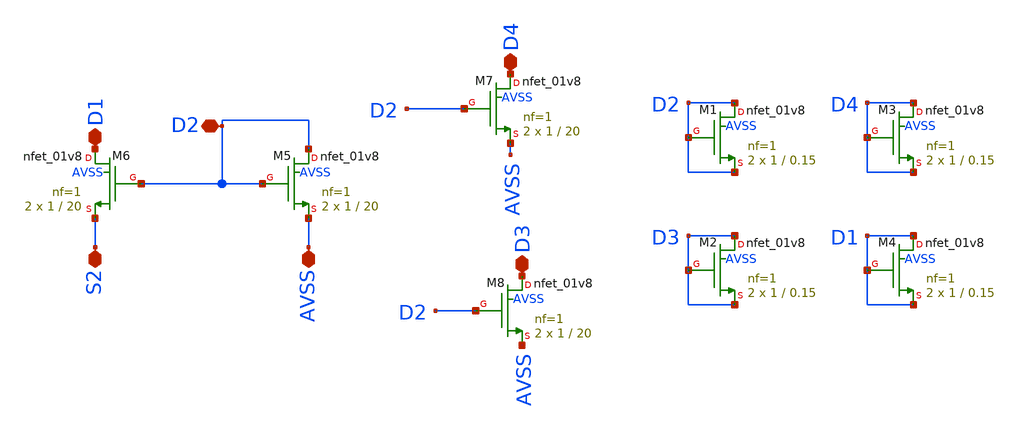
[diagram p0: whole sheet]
** sch_path: magic/nmos_tail_current.sch
**.subckt nmos_tail_current D1 S2 AVSS D2 D3 D4
*.iopin D1
*.iopin S2
*.iopin AVSS
*.iopin D2
*.iopin D3
*.iopin D4
XM6 D1 D2 S2 AVSS sky130_fd_pr__nfet_01v8 L=20 W=1 nf=1 ad='int((nf+1)/2) * W/nf * 0.29' as='int((nf+2)/2) * W/nf * 0.29'
+ pd='2*int((nf+1)/2) * (W/nf + 0.29)' ps='2*int((nf+2)/2) * (W/nf + 0.29)' nrd='0.29 / W' nrs='0.29 / W'
+ sa=0 sb=0 sd=0 mult=2 m=2
XM5 D2 D2 AVSS AVSS sky130_fd_pr__nfet_01v8 L=20 W=1 nf=1 ad='int((nf+1)/2) * W/nf * 0.29' as='int((nf+2)/2) * W/nf * 0.29'
+ pd='2*int((nf+1)/2) * (W/nf + 0.29)' ps='2*int((nf+2)/2) * (W/nf + 0.29)' nrd='0.29 / W' nrs='0.29 / W'
+ sa=0 sb=0 sd=0 mult=2 m=2
XM7 D4 D2 AVSS AVSS sky130_fd_pr__nfet_01v8 L=20 W=1 nf=1 ad='int((nf+1)/2) * W/nf * 0.29' as='int((nf+2)/2) * W/nf * 0.29'
+ pd='2*int((nf+1)/2) * (W/nf + 0.29)' ps='2*int((nf+2)/2) * (W/nf + 0.29)' nrd='0.29 / W' nrs='0.29 / W'
+ sa=0 sb=0 sd=0 mult=2 m=2
XM8 D3 D2 AVSS AVSS sky130_fd_pr__nfet_01v8 L=20 W=1 nf=1 ad='int((nf+1)/2) * W/nf * 0.29' as='int((nf+2)/2) * W/nf * 0.29'
+ pd='2*int((nf+1)/2) * (W/nf + 0.29)' ps='2*int((nf+2)/2) * (W/nf + 0.29)' nrd='0.29 / W' nrs='0.29 / W'
+ sa=0 sb=0 sd=0 mult=2 m=2
XM1 D2 D2 D2 AVSS sky130_fd_pr__nfet_01v8 L=0.15 W=1 nf=1 ad='int((nf+1)/2) * W/nf * 0.29' as='int((nf+2)/2) * W/nf * 0.29'
+ pd='2*int((nf+1)/2) * (W/nf + 0.29)' ps='2*int((nf+2)/2) * (W/nf + 0.29)' nrd='0.29 / W' nrs='0.29 / W'
+ sa=0 sb=0 sd=0 mult=2 m=2
XM2 D3 D3 D3 AVSS sky130_fd_pr__nfet_01v8 L=0.15 W=1 nf=1 ad='int((nf+1)/2) * W/nf * 0.29' as='int((nf+2)/2) * W/nf * 0.29'
+ pd='2*int((nf+1)/2) * (W/nf + 0.29)' ps='2*int((nf+2)/2) * (W/nf + 0.29)' nrd='0.29 / W' nrs='0.29 / W'
+ sa=0 sb=0 sd=0 mult=2 m=2
XM3 D4 D4 D4 AVSS sky130_fd_pr__nfet_01v8 L=0.15 W=1 nf=1 ad='int((nf+1)/2) * W/nf * 0.29' as='int((nf+2)/2) * W/nf * 0.29'
+ pd='2*int((nf+1)/2) * (W/nf + 0.29)' ps='2*int((nf+2)/2) * (W/nf + 0.29)' nrd='0.29 / W' nrs='0.29 / W'
+ sa=0 sb=0 sd=0 mult=2 m=2
XM4 D1 D1 D1 AVSS sky130_fd_pr__nfet_01v8 L=0.15 W=1 nf=1 ad='int((nf+1)/2) * W/nf * 0.29' as='int((nf+2)/2) * W/nf * 0.29'
+ pd='2*int((nf+1)/2) * (W/nf + 0.29)' ps='2*int((nf+2)/2) * (W/nf + 0.29)' nrd='0.29 / W' nrs='0.29 / W'
+ sa=0 sb=0 sd=0 mult=2 m=2
**.ends
.end
